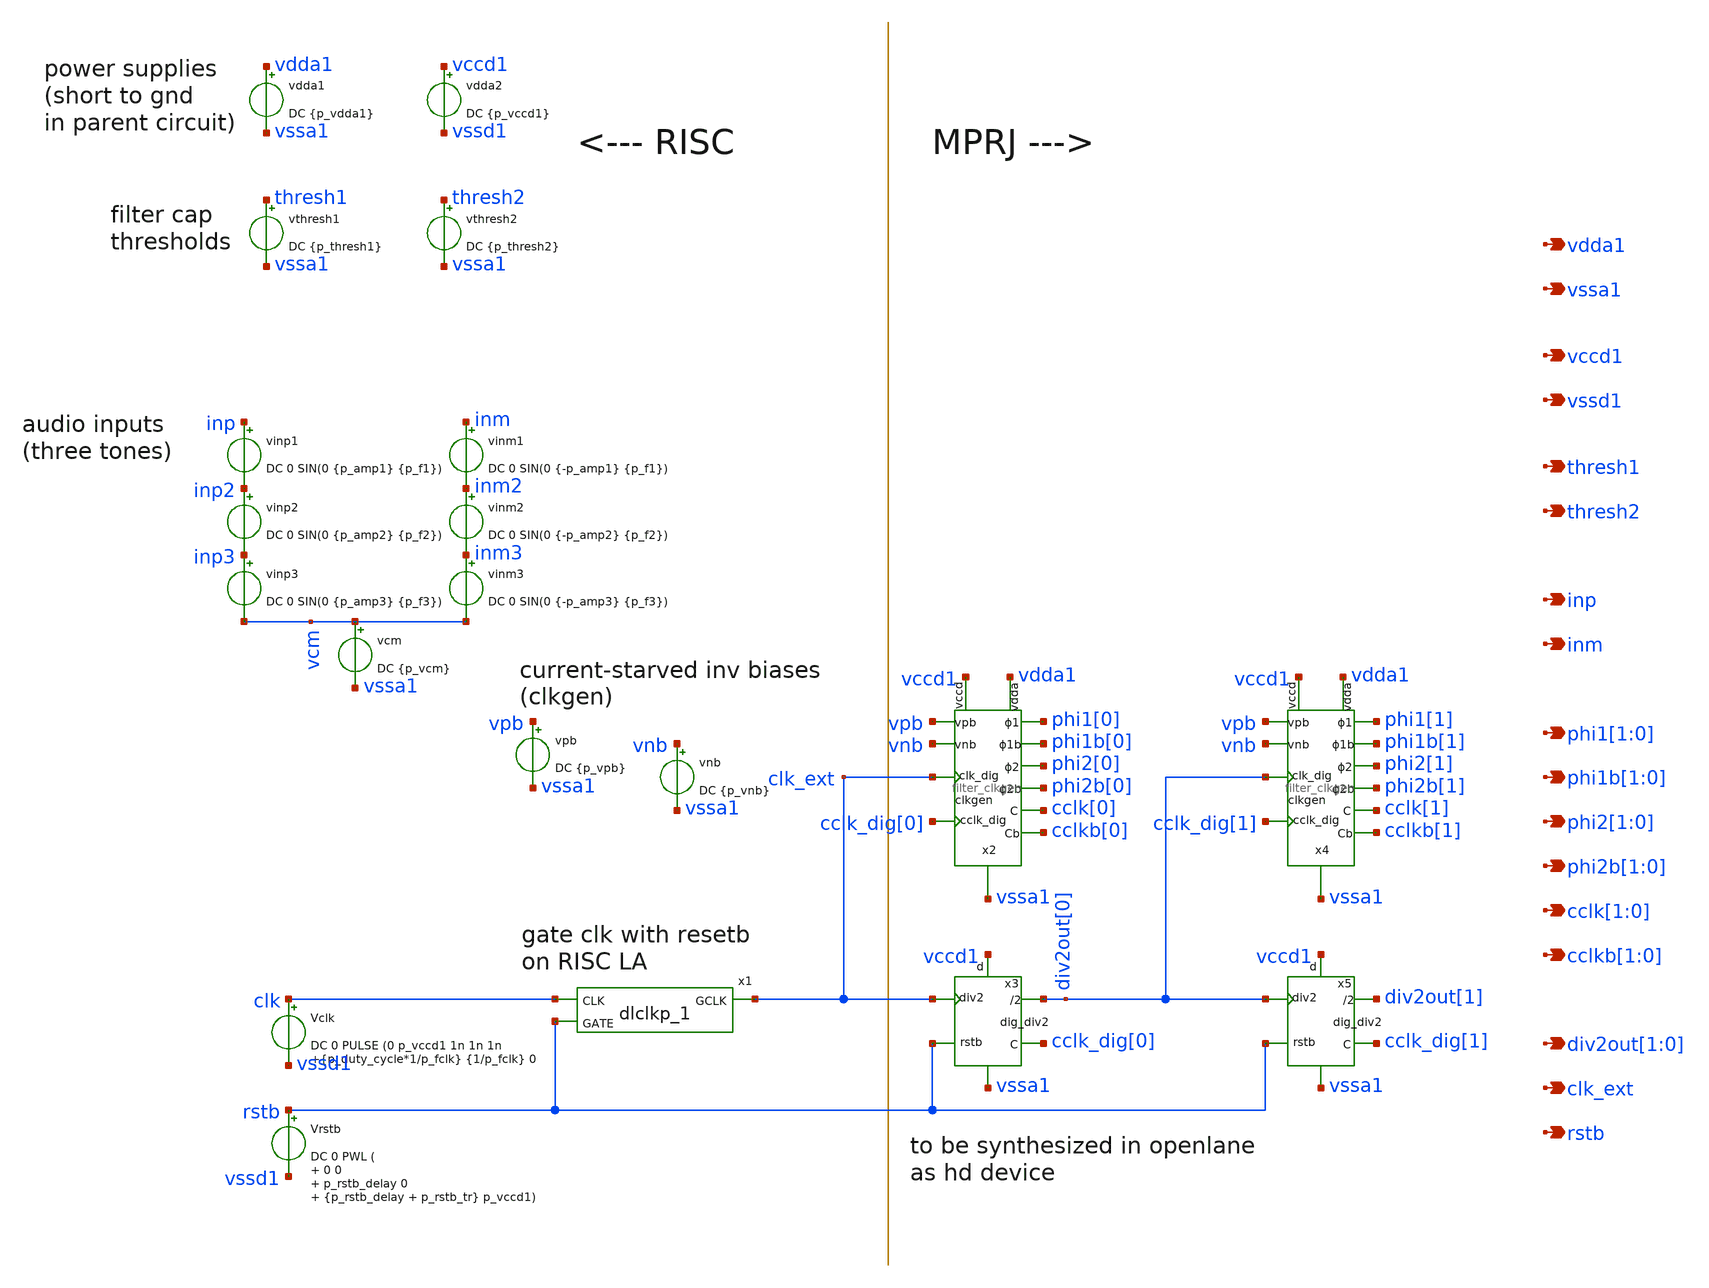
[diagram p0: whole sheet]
** sch_path: xschem/test_bench/risc_signals.sch
**.subckt risc_signals thresh1 thresh2 vdda1 vssa1 inp inm phi1[1],phi1[0] phi1b[1],phi1b[0] vccd1
*+ vssd1 div2out[1],div2out[0] rstb phi2[1],phi2[0] phi2b[1],phi2b[0] cclk[1],cclk[0] cclkb[1],cclkb[0]
*+ clk_ext
*.opin thresh1
*.opin thresh2
*.opin vdda1
*.opin vssa1
*.opin inp
*.opin inm
*.opin phi1[1],phi1[0]
*.opin phi1b[1],phi1b[0]
*.opin vccd1
*.opin vssd1
*.opin div2out[1],div2out[0]
*.opin rstb
*.opin phi2[1],phi2[0]
*.opin phi2b[1],phi2b[0]
*.opin cclk[1],cclk[0]
*.opin cclkb[1],cclkb[0]
*.opin clk_ext
vdda1 vdda1 vssa1 DC {p_vdda1}
vthresh1 thresh1 vssa1 DC {p_thresh1}
vthresh2 thresh2 vssa1 DC {p_thresh2}
vinp1 inp inp2 DC 0 SIN(0 {p_amp1} {p_f1})
vinm1 inm inm2 DC 0 SIN(0 {-p_amp1} {p_f1})
vpb vpb vssa1 DC {p_vpb}
vnb vnb vssa1 DC {p_vnb}
vinp2 inp2 inp3 DC 0 SIN(0 {p_amp2} {p_f2})
vinp3 inp3 vcm DC 0 SIN(0 {p_amp3} {p_f3})
vinm2 inm2 inm3 DC 0 SIN(0 {-p_amp2} {p_f2})
vinm3 inm3 vcm DC 0 SIN(0 {-p_amp3} {p_f3})
vcm vcm vssa1 DC {p_vcm}
vdda2 vccd1 vssd1 DC {p_vccd1}
Vclk clk vssd1 DC 0 PULSE (0 p_vccd1 1n 1n 1n {p_duty_cycle*1/p_fclk} {1/p_fclk} 0
Vrstb rstb vssd1 DC 0 PWL ( 0 0 p_rstb_delay 0 {p_rstb_delay + p_rstb_tr} p_vccd1)
x1 clk rstb vssd1 vssd1 vccd1 vccd1 clk_ext sky130_fd_sc_hd__dlclkp_1
x2 cclk_dig[0] phi2b[0] phi2[0] phi1b[0] phi1[0] cclkb[0] cclk[0] vpb vnb vdda1 vssa1 vccd1 clk_ext
+ filter_clkgen
x3 rstb cclk_dig[0] div2out[0] vccd1 vssa1 clk_ext dig_div2
x4 cclk_dig[1] phi2b[1] phi2[1] phi1b[1] phi1[1] cclkb[1] cclk[1] vpb vnb vdda1 vssa1 vccd1
+ div2out[0] filter_clkgen
x5 rstb cclk_dig[1] div2out[1] vccd1 vssa1 div2out[0] dig_div2
**.ends
.end
